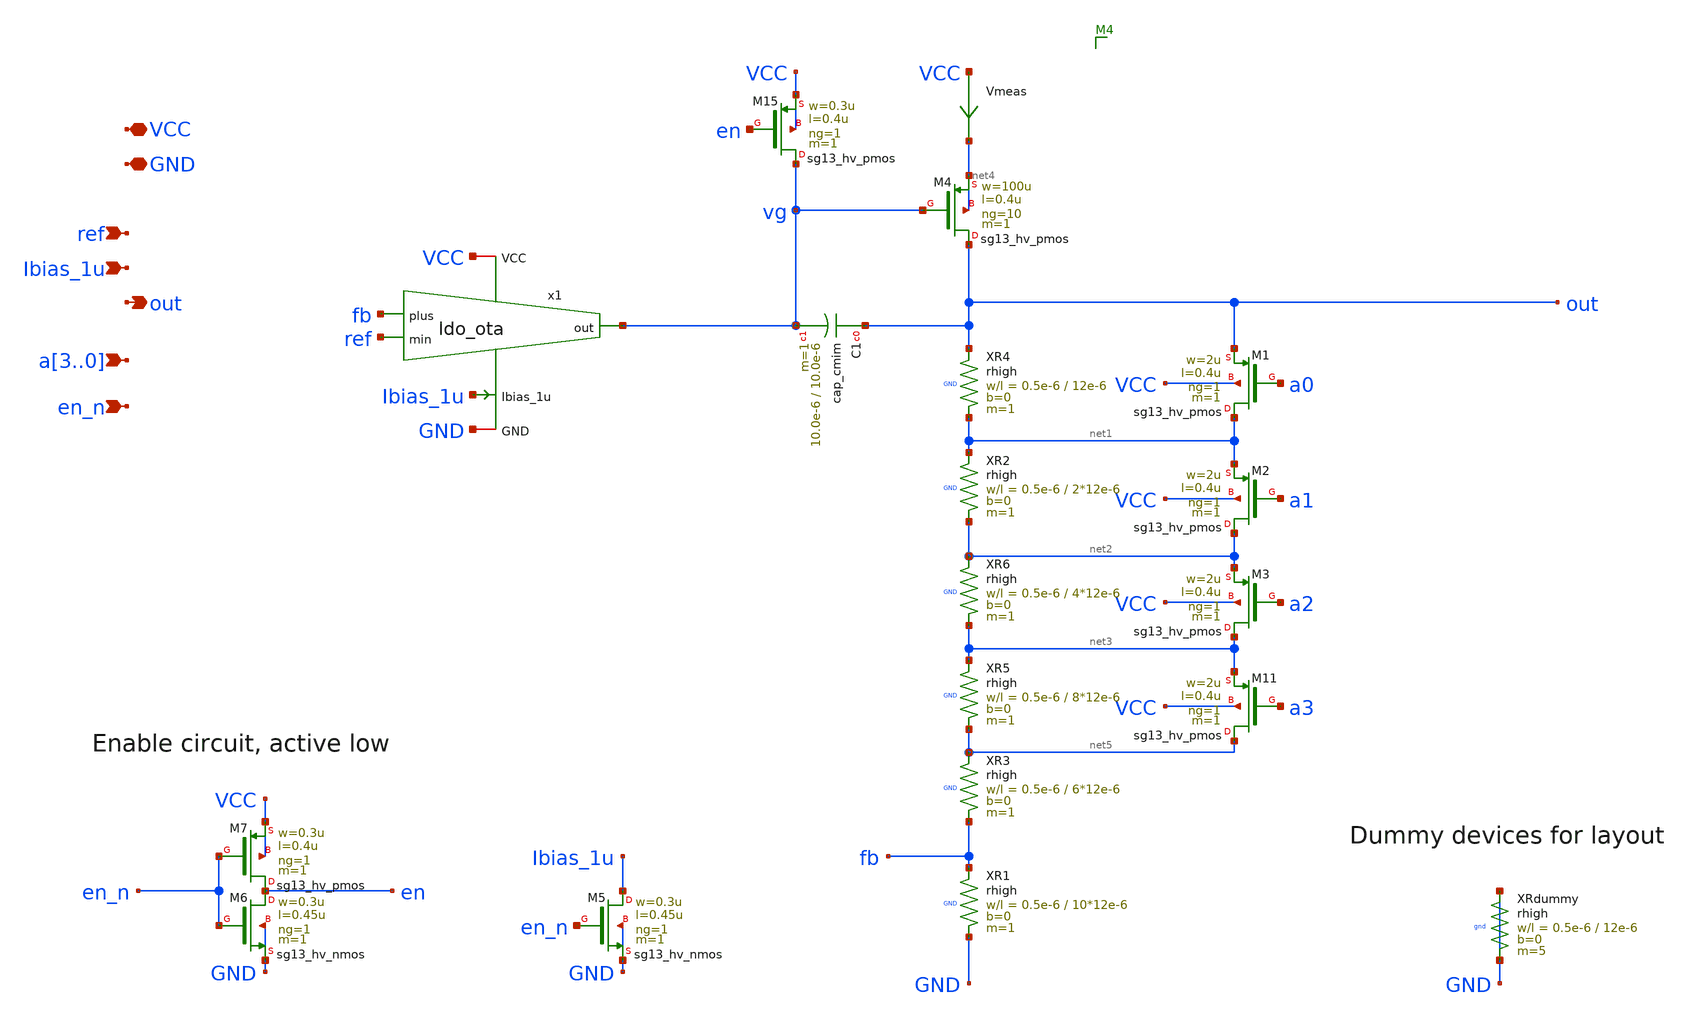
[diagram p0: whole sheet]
** sch_path: FLDO/design_data/xschem/ldo_binary.sch
**.subckt ldo_binary VCC GND ref Ibias_1u out a3,a2,a1,a0 en_n
*.iopin VCC
*.iopin GND
*.ipin ref
*.ipin Ibias_1u
*.opin out
*.ipin a3,a2,a1,a0
*.ipin en_n
XR4 net1 out GND rhigh w=0.5e-6 l=12e-6 m=1 b=0
XM1 net1 a0 out VCC sg13_hv_pmos w=2u l=0.4u ng=1 m=1 mm_ok=1
XM2 net2 a1 net1 VCC sg13_hv_pmos w=2u l=0.4u ng=1 m=1 mm_ok=1
XM3 net3 a2 net2 VCC sg13_hv_pmos w=2u l=0.4u ng=1 m=1 mm_ok=1
XM4 out vg net4 net4 sg13_hv_pmos w=100u l=0.4u ng=10 m=1 mm_ok=1
Vmeas VCC net4 0
.save i(vmeas)
XC1 out vg cap_cmim w=10.0e-6 l=10.0e-6 m=1
XM11 net5 a3 net3 VCC sg13_hv_pmos w=2u l=0.4u ng=1 m=1 mm_ok=1
XM15 vg en VCC VCC sg13_hv_pmos w=0.3u l=0.4u ng=1 m=1 mm_ok=1
x1 VCC GND Ibias_1u fb ref vg ldo_ota
XM5 Ibias_1u en_n GND GND sg13_hv_nmos w=0.3u l=0.45u ng=1 m=1 mm_ok=1
XM6 en en_n GND GND sg13_hv_nmos w=0.3u l=0.45u ng=1 m=1 mm_ok=1
XM7 en en_n VCC VCC sg13_hv_pmos w=0.3u l=0.4u ng=1 m=1 mm_ok=1
XRdummy GND GND gnd rhigh w=0.5e-6 l=12e-6 m=5 b=0
XR2 net2 net1 GND rhigh w=0.5e-6 l=2*12e-6 m=1 b=0
XR6 net3 net2 GND rhigh w=0.5e-6 l=4*12e-6 m=1 b=0
XR5 net5 net3 GND rhigh w=0.5e-6 l=8*12e-6 m=1 b=0
XR3 fb net5 GND rhigh w=0.5e-6 l=6*12e-6 m=1 b=0
XR1 GND fb GND rhigh w=0.5e-6 l=10*12e-6 m=1 b=0
**.ends

* expanding   symbol:  ldo_ota.sym # of pins=6
** sym_path: FLDO/design_data/xschem/ldo_ota.sym
** sch_path: FLDO/design_data/xschem/ldo_ota.sch
.subckt ldo_ota VCC GND Ibias_1u plus min out
*.iopin VCC
*.iopin GND
*.ipin plus
*.ipin min
*.opin out
*.ipin Ibias_1u
XM5 vbp plus tail GND sg13_hv_nmos w=3u l=2u ng=3 m=1 mm_ok=1
XM6 out min tail GND sg13_hv_nmos w=3u l=2u ng=3 m=1 mm_ok=1
XM7 tail Ibias_1u GND GND sg13_hv_nmos w=1u l=2u ng=1 m=2 mm_ok=1
XM8 Ibias_1u Ibias_1u GND GND sg13_hv_nmos w=1u l=2u ng=1 m=1 mm_ok=1
XM9 out vbp VCC VCC sg13_hv_pmos w=2u l=2u ng=2 m=1 mm_ok=1
XM10 vbp vbp VCC VCC sg13_hv_pmos w=2u l=2u ng=2 m=1 mm_ok=1
XMdummy0 GND Ibias_1u GND GND sg13_hv_nmos w=1u l=2u ng=1 m=2 mm_ok=1
XMdummy1 tail tail tail GND sg13_hv_nmos w=1u l=2u ng=1 m=4 mm_ok=1
XMdummyP VCC vbp VCC VCC sg13_hv_pmos w=1u l=2u ng=1 m=2 mm_ok=1
.ends

.end
